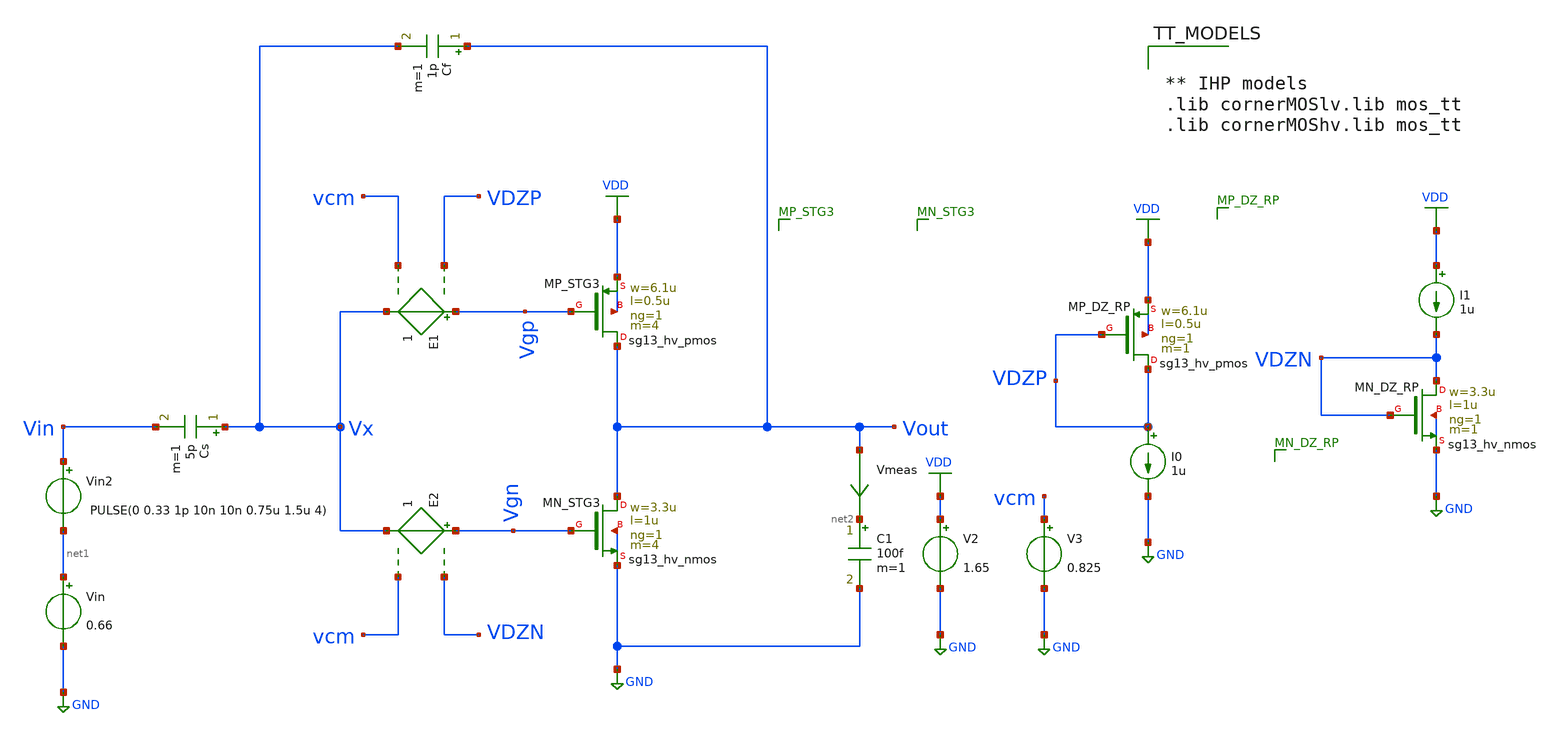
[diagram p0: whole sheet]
** sch_path: VLSI25/submitted_notebooks/Wrøngm/Schematics/INV_ota_rongm_try1.sch
**.subckt INV_ota_rongm_try1
Vin net1 GND 0.66
E1 Vgp Vx VDZP vcm 1
E2 Vgn Vx VDZN vcm 1
I0 VDZP GND 1u
I1 VDD VDZN 1u
V2 VDD GND 1.65
V3 vcm GND 0.825
XMP_STG3 Vout Vgp VDD VDD sg13_hv_pmos w=6.1u l=0.5u ng=1 m=4 mm_ok=1
XMP_DZ_RP VDZP VDZP VDD VDD sg13_hv_pmos w=6.1u l=0.5u ng=1 m=1 mm_ok=1
XMN_STG3 Vout Vgn GND GND sg13_hv_nmos w=3.3u l=1u ng=1 m=4 mm_ok=1
XMN_DZ_RP VDZN VDZN GND GND sg13_hv_nmos w=3.3u l=1u ng=1 m=1 mm_ok=1
Cs Vx Vin 5p m=1
Cf Vout Vx 1p m=1
C1 net2 GND 100f m=1
Vmeas Vout net2 0
.save i(vmeas)
Vin2 Vin net1 PULSE(0 0.33 1p 10n 10n 0.75u 1.5u 4)
**** begin user architecture code


** IHP models
.lib cornerMOSlv.lib mos_tt
.lib cornerMOShv.lib mos_tt




.save @n.xmp_stg3.nsg13_hv_pmos[gm]
.save @n.xmp_stg3.nsg13_hv_pmos[gds]
.save @n.xmp_stg3.nsg13_hv_pmos[vth]
.save @n.xmp_stg3.nsg13_hv_pmos[vdss]
.save @n.xmp_stg3.nsg13_hv_pmos[cgg]
.save @n.xmp_stg3.nsg13_hv_pmos[cgsol]
.save @n.xmp_stg3.nsg13_hv_pmos[cgdol]
.save @n.xmp_dz_rp.nsg13_hv_pmos[gm]
.save @n.xmp_dz_rp.nsg13_hv_pmos[gds]
.save @n.xmp_dz_rp.nsg13_hv_pmos[vth]
.save @n.xmp_dz_rp.nsg13_hv_pmos[vdss]
.save @n.xmp_dz_rp.nsg13_hv_pmos[cgg]
.save @n.xmp_dz_rp.nsg13_hv_pmos[cgsol]
.save @n.xmp_dz_rp.nsg13_hv_pmos[cgdol]
.save @n.xmn_stg3.nsg13_hv_nmos[gm]
.save @n.xmn_stg3.nsg13_hv_nmos[gds]
.save @n.xmn_stg3.nsg13_hv_nmos[vth]
.save @n.xmn_stg3.nsg13_hv_nmos[vdss]
.save @n.xmn_stg3.nsg13_hv_nmos[cgg]
.save @n.xmn_stg3.nsg13_hv_nmos[cgsol]
.save @n.xmn_stg3.nsg13_hv_nmos[cgdol]
.save @n.xmn_dz_rp.nsg13_hv_nmos[gm]
.save @n.xmn_dz_rp.nsg13_hv_nmos[gds]
.save @n.xmn_dz_rp.nsg13_hv_nmos[vth]
.save @n.xmn_dz_rp.nsg13_hv_nmos[vdss]
.save @n.xmn_dz_rp.nsg13_hv_nmos[cgg]
.save @n.xmn_dz_rp.nsg13_hv_nmos[cgsol]
.save @n.xmn_dz_rp.nsg13_hv_nmos[cgdol]





.ic v(vout)=0.825 v(Vin)=0.825 v(vgn)=0.67213 v(vgp)=0.99954 v(Vx)=0.825
.option wnflag=1
.option savecurrents
.temp 27
.control
save all
write INV_ota_rongm_try1.raw
set appendwrite
op
write INV_ota_rongm_try1.raw
**dc V1 0 1.65 1m
tran 1n 3u 0.1n
**ac dec 20 1 1e10
plot v(vout) v(vin)
plot v(vout)
plot v(vin)
plot v(vx)
plot v(vgp)
plot v(vgn)
plot @n.xmp_stg3.nsg13_hv_pmos[ids] @n.xmn_stg3.nsg13_hv_nmos[ids]
plot @n.xmp_stg3.nsg13_hv_pmos[ids]
plot @n.xmn_stg3.nsg13_hv_nmos[ids]
plot @c1[i]
wrdata /foss/designs/CAC/Inverter-OTA/Ron_gm/inv-OA-try1_Error3.txt v(vout) v(vx) v(vin)
+ @n.xmp_stg3.nsg13_hv_pmos[ids]  @n.xmn_stg3.nsg13_hv_nmos[ids] @c1[i]
.endc


**** end user architecture code
**.ends
.GLOBAL GND
.GLOBAL VDD
.end
